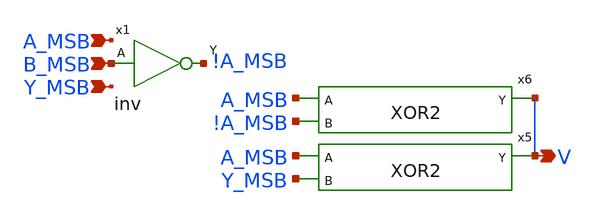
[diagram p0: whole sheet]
** sch_path: design/xschem/ZV_FLAG/V_FLAG.sch
**.subckt V_FLAG V A_MSB B_MSB Y_MSB
*.opin V
*.ipin A_MSB
*.ipin B_MSB
*.ipin Y_MSB
x5 A_MSB Y_MSB V VSS VDD XOR2
x6 A_MSB !A_MSB V VSS VDD XOR2
x1 B_MSB VSS VDD !A_MSB inv
**.ends
.end
